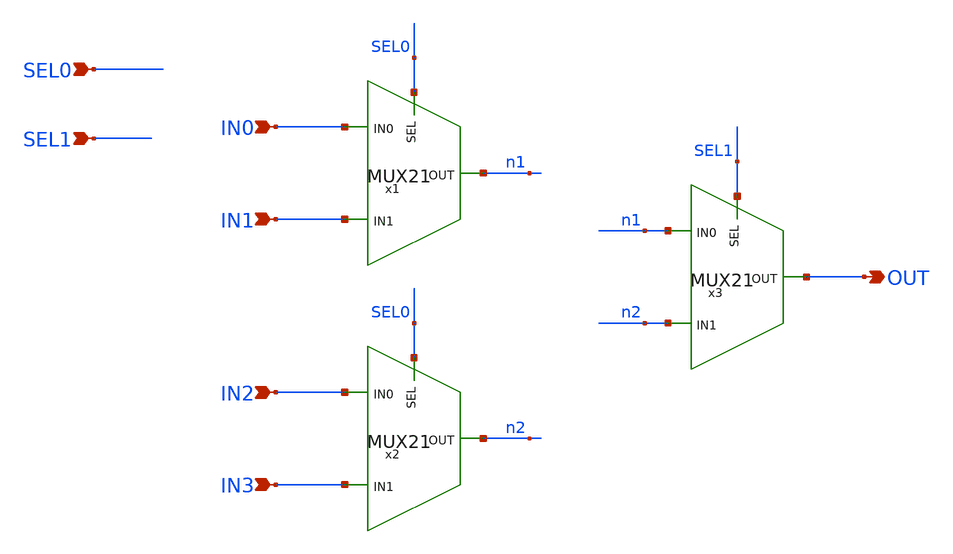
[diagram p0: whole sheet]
** sch_path: MUX41.sch
**.subckt MUX41 IN0 IN1 SEL0 SEL1 IN2 IN3 OUT
*.ipin IN0
*.ipin IN1
*.ipin SEL0
*.ipin SEL1
*.ipin IN2
*.ipin IN3
*.opin OUT
x1 IN0 SEL0 n1 IN1 MUX21
x2 IN2 SEL0 n2 IN3 MUX21
x3 n1 SEL1 OUT n2 MUX21
**.ends
.end
